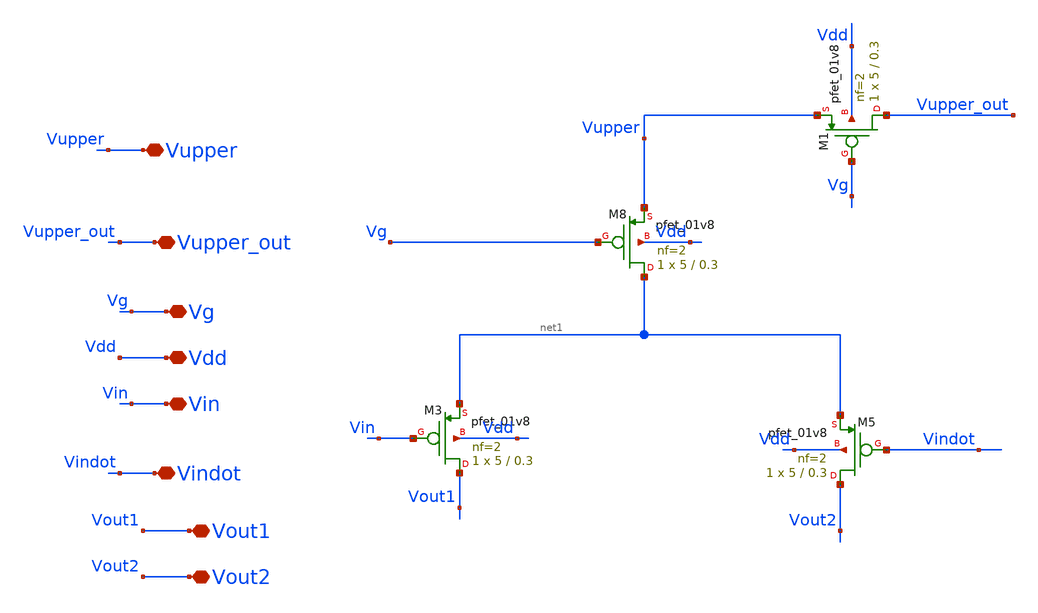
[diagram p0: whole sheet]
** sch_path: xschem/dac_inside_tt_v2.sch
**.subckt dac_inside_tt_v2 Vg Vin Vdd Vout1 Vout2 Vupper Vindot Vupper_out
*.iopin Vg
*.iopin Vin
*.iopin Vdd
*.iopin Vout1
*.iopin Vout2
*.iopin Vupper
*.iopin Vindot
*.iopin Vupper_out
XM8 net1 Vg Vupper Vdd sky130_fd_pr__pfet_01v8 L=0.3 W=5 nf=2 ad='int((nf+1)/2) * W/nf * 0.29' as='int((nf+2)/2) * W/nf * 0.29'
+ pd='2*int((nf+1)/2) * (W/nf + 0.29)' ps='2*int((nf+2)/2) * (W/nf + 0.29)' nrd='0.29 / W' nrs='0.29 / W'
+ sa=0 sb=0 sd=0 mult=1 m=1
XM5 Vout2 Vindot net1 Vdd sky130_fd_pr__pfet_01v8 L=0.3 W=5 nf=2 ad='int((nf+1)/2) * W/nf * 0.29' as='int((nf+2)/2) * W/nf * 0.29'
+ pd='2*int((nf+1)/2) * (W/nf + 0.29)' ps='2*int((nf+2)/2) * (W/nf + 0.29)' nrd='0.29 / W' nrs='0.29 / W'
+ sa=0 sb=0 sd=0 mult=1 m=1
XM3 Vout1 Vin net1 Vdd sky130_fd_pr__pfet_01v8 L=0.3 W=5 nf=2 ad='int((nf+1)/2) * W/nf * 0.29' as='int((nf+2)/2) * W/nf * 0.29'
+ pd='2*int((nf+1)/2) * (W/nf + 0.29)' ps='2*int((nf+2)/2) * (W/nf + 0.29)' nrd='0.29 / W' nrs='0.29 / W'
+ sa=0 sb=0 sd=0 mult=1 m=1
XM1 Vupper_out Vg Vupper Vdd sky130_fd_pr__pfet_01v8 L=0.3 W=5 nf=2 ad='int((nf+1)/2) * W/nf * 0.29'
+ as='int((nf+2)/2) * W/nf * 0.29' pd='2*int((nf+1)/2) * (W/nf + 0.29)' ps='2*int((nf+2)/2) * (W/nf + 0.29)'
+ nrd='0.29 / W' nrs='0.29 / W' sa=0 sb=0 sd=0 mult=1 m=1
**.ends
.end
